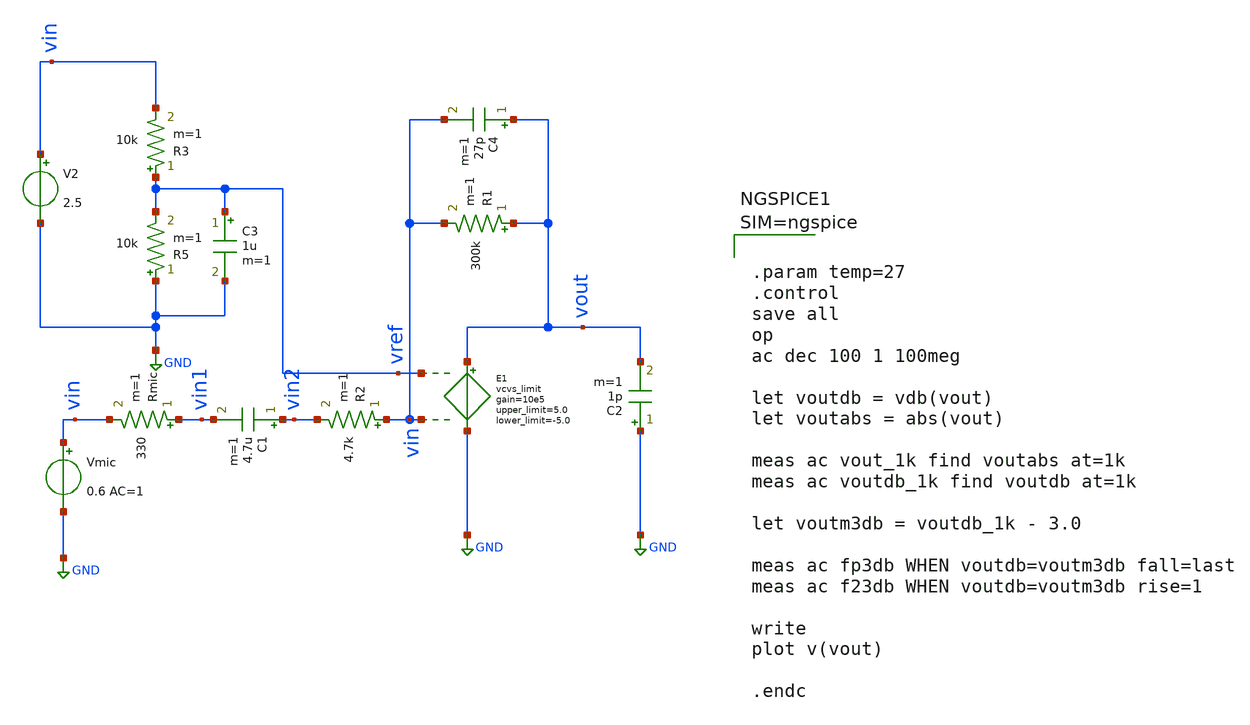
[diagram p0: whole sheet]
** sch_path: week-1/xschem/untitled.sch
**.subckt untitled
Vmic vin GND 0.6 AC=1
Rmic vin1 vin 330 m=1
R2 vin vin2 4.7k m=1
C1 vin2 vin1 4.7u m=1
V2 vin GND 2.5
E1 %vd( vref vin ) %vd( vout GND ) E1
.model E1 limit ( gain=10e5 out_lower_limit=-5.0 out_upper_limit=5.0 )
C2 GND vout 1p m=1
C3 vref GND 1u m=1
R3 vref vin 10k m=1
R5 GND vref 10k m=1
C4 vout vin 27p m=1
R1 vout vin 300k m=1
**** begin user architecture code



.param temp=27
.control
save all
op
ac dec 100 1 100meg

let voutdb = vdb(vout)
let voutabs = abs(vout)

meas ac vout_1k find voutabs at=1k
meas ac voutdb_1k find voutdb at=1k

let voutm3db = voutdb_1k - 3.0

meas ac fp3db WHEN voutdb=voutm3db fall=last
meas ac f23db WHEN voutdb=voutm3db rise=1

write
plot v(vout)

.endc


**** end user architecture code
**.ends
.GLOBAL GND
.end
